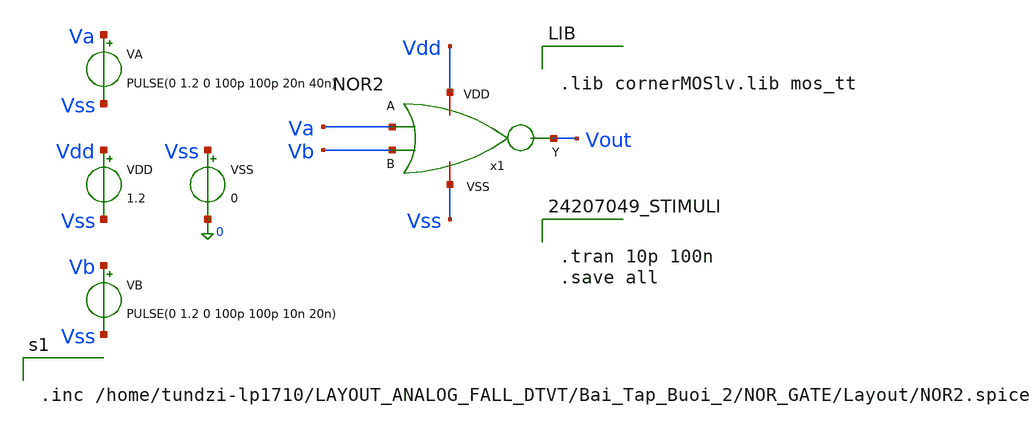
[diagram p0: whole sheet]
** sch_path: logic_gate/NOR2/LAYOUT_POST-SIMULATION/NOR2_tb.sch
**.subckt NOR2_tb
VDD Vdd Vss 1.2
VSS Vss 0 0
VA Va Vss PULSE(0 1.2 0 100p 100p 20n 40n)
VB Vb Vss PULSE(0 1.2 0 100p 100p 10n 20n)
x1 Vdd Vss Va Vb Vout NOR2
**** begin user architecture code


.lib cornerMOSlv.lib mos_tt




.tran 10p 100n
.save all




.inc /home/tundzi-lp1710/LAYOUT_ANALOG_FALL_DTVT/Bai_Tap_Buoi_2/NOR_GATE/Layout/NOR2.spice


**** end user architecture code
**.ends
.end
